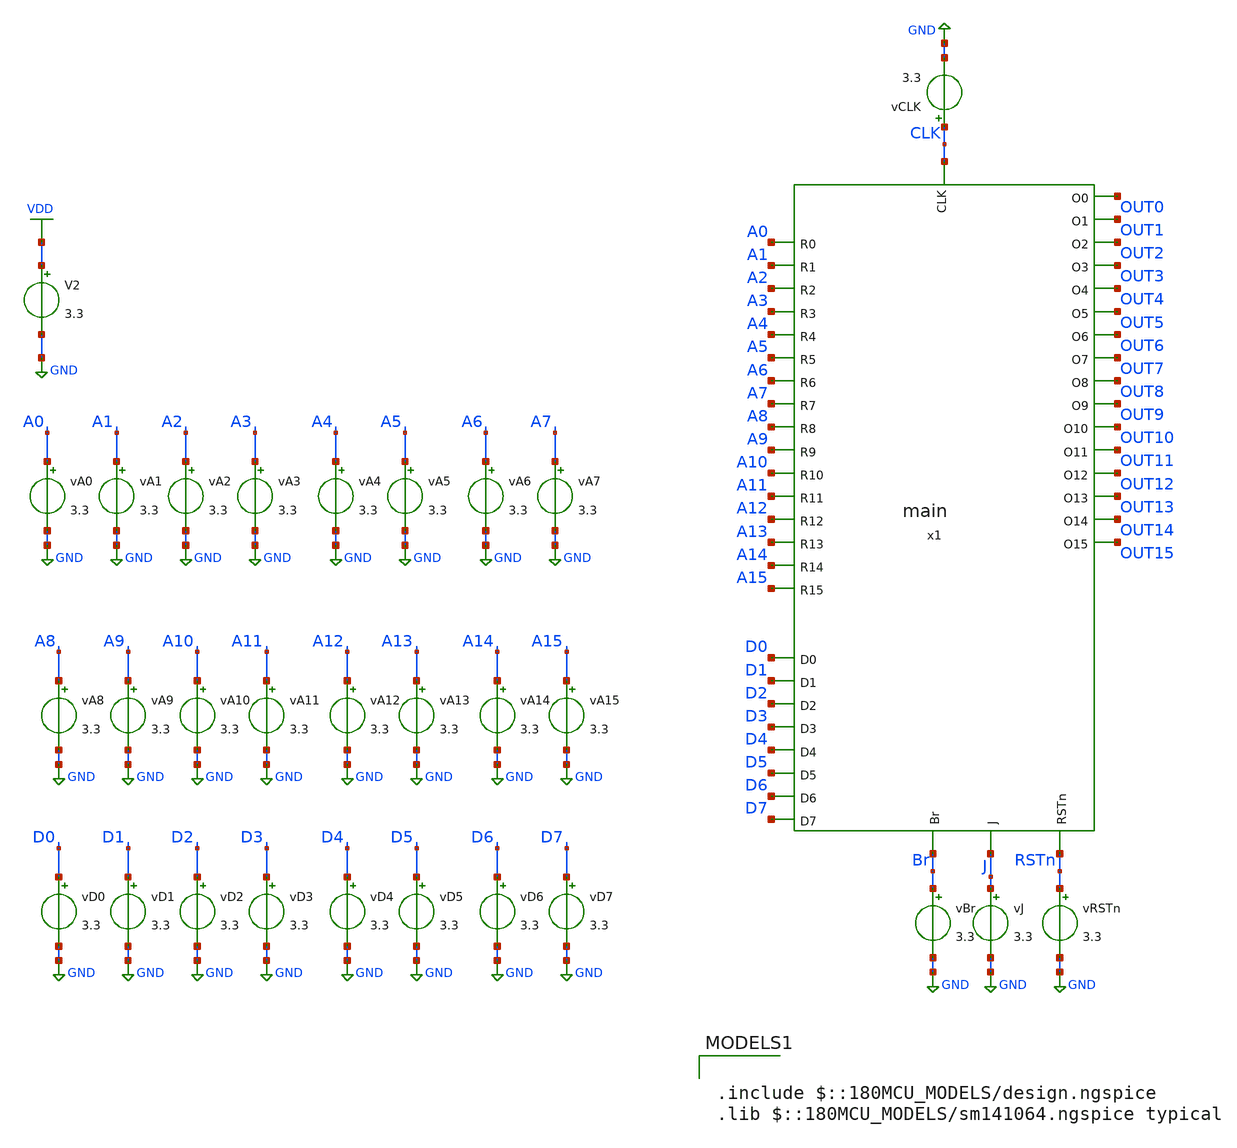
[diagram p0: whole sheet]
** sch_path: tbs/critical_path_prePEX.sch
**.subckt critical_path_prePEX
vA0 A0 GND 3.3
vA1 A1 GND 3.3
vA2 A2 GND 3.3
vA3 A3 GND 3.3
vA4 A4 GND 3.3
vA5 A5 GND 3.3
vA6 A6 GND 3.3
vA7 A7 GND 3.3
vA8 A8 GND 3.3
vA9 A9 GND 3.3
vA10 A10 GND 3.3
vA11 A11 GND 3.3
vA12 A12 GND 3.3
vA13 A13 GND 3.3
vA14 A14 GND 3.3
vA15 A15 GND 3.3
V2 VDD GND 3.3
vD0 D0 GND 3.3
vD1 D1 GND 3.3
vD2 D2 GND 3.3
vD3 D3 GND 3.3
vD4 D4 GND 3.3
vD5 D5 GND 3.3
vD6 D6 GND 3.3
vD7 D7 GND 3.3
vCLK CLK GND 3.3
vRSTn RSTn GND 3.3
vJ J GND 3.3
vBr Br GND 3.3
x1 J A0 CLK A1 A2 OUT4 OUT8 A3 OUT12 OUT0 A4 OUT5 OUT9 A5 OUT1 OUT13 A6 OUT10 OUT2 A7 OUT14 OUT6 A8
+ OUT11 OUT15 A9 OUT7 OUT3 A10 A11 A12 A13 A14 A15 RSTn Br D0 D1 D2 D3 D4 D5 D6 D7 main
**** begin user architecture code

.include $::180MCU_MODELS/design.ngspice
.lib $::180MCU_MODELS/sm141064.ngspice typical



.control
let vlow = 0
let vhigh = 3.3

* --- Setup Inputs ---
* A = 1111111111111111 (65535)
alter vA15 = $&vhigh
alter vA14 = $&vhigh
alter vA13 = $&vhigh
alter vA12 = $&vhigh
alter vA11 = $&vhigh
alter vA10 = $&vhigh
alter vA9  = $&vhigh
alter vA8  = $&vhigh
alter vA7  = $&vhigh
alter vA6  = $&vhigh
alter vA5  = $&vhigh
alter vA4  = $&vhigh
alter vA3  = $&vhigh
alter vA2  = $&vhigh
alter vA1  = $&vhigh
alter vA0  = $&vhigh

* D = 00001111 (15)
alter vD7 = $&vlow
alter vD6 = $&vlow
alter vD5 = $&vlow
alter vD4 = $&vlow
alter vD3 = $&vlow
alter vD2 = $&vlow
alter vD1 = $&vlow
alter vD0 = $&vlow

* --- Control Signals ---
alter @vJ[pulse] = [ $&vlow $&vhigh 1n 1n 1n 20n 40n ]

* Setup vCLK as a pulse: Initial, Pulse, Delay, Rise, Fall, Width, Period
* Example: 10ns period, 50% duty cycle
alter @vCLK[pulse] = [ $&vlow $&vhigh 10n 1n 1n 5n 20n ]

* Setup vBr as a pulse: This triggers the branch offset.
* We delay it so it's active during a specific clock edge.
alter @vBr[pulse] = [ $&vhigh $&vlow 25n 1n 1n 20n 40n ]
alter @vRSTn[pulse] = [ $&vhigh $&vlow 1n 1n 1n 1n 40n ]
* --- Run Simulation ---
tran 1n 40n
* --- Measurement at 30ns ---
* (Assuming the branch has processed and state is stable)
meas tran v1_0  find v(OUT0)  at=30n
meas tran v1_1  find v(OUT1)  at=30n
meas tran v1_2  find v(OUT2)  at=30n
meas tran v1_3  find v(OUT3)  at=30n
meas tran v1_4  find v(OUT4)  at=30n
meas tran v1_5  find v(OUT5)  at=30n
meas tran v1_6  find v(OUT6)  at=30n
meas tran v1_7  find v(OUT7)  at=30n
meas tran v1_8  find v(OUT8)  at=30n
meas tran v1_9  find v(OUT9)  at=30n
meas tran v1_10 find v(OUT10) at=30n
meas tran v1_11 find v(OUT11) at=30n
meas tran v1_12 find v(OUT12) at=30n
meas tran v1_13 find v(OUT13) at=30n
meas tran v1_14 find v(OUT14) at=30n
meas tran v1_15 find v(OUT15) at=30n

* --- Result Processing ---
let res1 = 0
if v1_0 > 1.6
  let res1 = res1 + 1
end
if v1_1 > 1.6
  let res1 = res1 + 2
end
if v1_2 > 1.6
  let res1 = res1 + 4
end
if v1_3 > 1.6
  let res1 = res1 + 8
end
if v1_4 > 1.6
  let res1 = res1 + 16
end
if v1_5 > 1.6
  let res1 = res1 + 32
end
if v1_6 > 1.6
  let res1 = res1 + 64
end
if v1_7 > 1.6
  let res1 = res1 + 128
end
if v1_8 > 1.6
  let res1 = res1 + 256
end
if v1_9 > 1.6
  let res1 = res1 + 512
end
if v1_10 > 1.6
  let res1 = res1 + 1024
end
if v1_11 > 1.6
  let res1 = res1 + 2048
end
if v1_12 > 1.6
  let res1 = res1 + 4096
end
if v1_13 > 1.6
  let res1 = res1 + 8192
end
if v1_14 > 1.6
  let res1 = res1 + 16384
end
if v1_15 > 1.6
  let res1 = res1 + 32768
end

echo res_value:
print res1
meas tran read_fall TRIG v(Br) VAL=1.65 FALL=1 TARG v(OUT15) VAL=1.65 FALL=1 FROM=20n TO=30n
.endc


**** end user architecture code
**.ends
.GLOBAL GND
.GLOBAL VDD
.end
